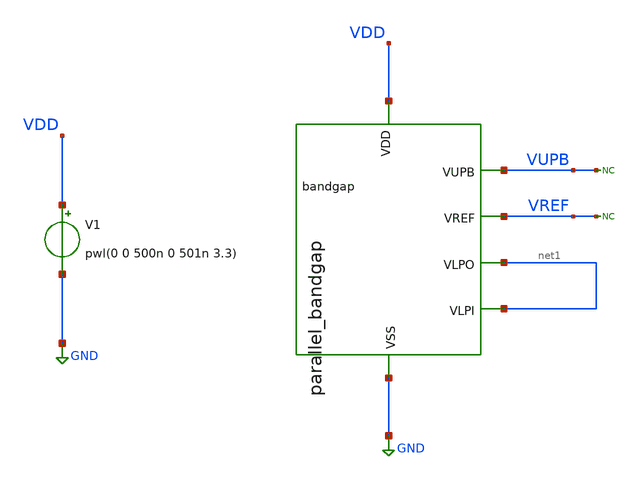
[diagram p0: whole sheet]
** sch_path: testbenches/parallel_bandgap_tran.sch
**.subckt parallel_bandgap_tran
bandgap VDD VUPB VREF net1 net1 GND parallel_bandgap
V1 VDD GND pwl(0 0 500n 0 501n 3.3)
.save i(v1)
* noconn VUPB
* noconn VREF
**.ends

* expanding   symbol:  parallel_bandgap.sym # of pins=6
** sym_path: designs/parallel_bandgap.sym
** sch_path: designs/parallel_bandgap.sch
.subckt parallel_bandgap VDD VUPB VREF VLPI VLPO VSS
*.ipin VDD
*.ipin VSS
*.opin VUPB
*.opin VREF
*.opin VLPO
*.ipin VLPI
XM1 net3 VUPB VDD VDD sky130_fd_pr__pfet_01v8_lvt L=8 W=50 nf=1 ad='int((nf+1)/2) * W/nf * 0.29' as='int((nf+2)/2) * W/nf * 0.29'
+ pd='2*int((nf+1)/2) * (W/nf + 0.29)' ps='2*int((nf+2)/2) * (W/nf + 0.29)' nrd='0.29 / W' nrs='0.29 / W'
+ sa=0 sb=0 sd=0 mult=1 m=1
XM2 net2 VUPB VDD VDD sky130_fd_pr__pfet_01v8_lvt L=8 W=50 nf=1 ad='int((nf+1)/2) * W/nf * 0.29' as='int((nf+2)/2) * W/nf * 0.29'
+ pd='2*int((nf+1)/2) * (W/nf + 0.29)' ps='2*int((nf+2)/2) * (W/nf + 0.29)' nrd='0.29 / W' nrs='0.29 / W'
+ sa=0 sb=0 sd=0 mult=1 m=1
XQ1 net12 VLPI net1 VSS sky130_fd_pr__npn_05v5_w1p00l2p00
XQ2 net11 VLPO VSS VSS sky130_fd_pr__npn_05v5_w1p00l2p00
XR1 VSS net1 VSS sky130_fd_pr__res_high_po_1p41 L=260 mult=1 m=1
XQ3 net4 VBE VSS VSS sky130_fd_pr__npn_05v5_w1p00l2p00
XR2 VSS VBE VSS sky130_fd_pr__res_high_po_1p41 L=2400 mult=1 m=1
XM4 VBE VCCAS net6 VDD sky130_fd_pr__pfet_01v8_lvt L=8 W=50 nf=1 ad='int((nf+1)/2) * W/nf * 0.29' as='int((nf+2)/2) * W/nf * 0.29'
+ pd='2*int((nf+1)/2) * (W/nf + 0.29)' ps='2*int((nf+2)/2) * (W/nf + 0.29)' nrd='0.29 / W' nrs='0.29 / W'
+ sa=0 sb=0 sd=0 mult=1 m=1
XM5 VCBIAS VCCAS net5 VDD sky130_fd_pr__pfet_01v8_lvt L=8 W=50 nf=1 ad='int((nf+1)/2) * W/nf * 0.29'
+ as='int((nf+2)/2) * W/nf * 0.29' pd='2*int((nf+1)/2) * (W/nf + 0.29)' ps='2*int((nf+2)/2) * (W/nf + 0.29)'
+ nrd='0.29 / W' nrs='0.29 / W' sa=0 sb=0 sd=0 mult=1 m=1
XM6 VCCAS net4 VSS VSS sky130_fd_pr__nfet_01v8 L=4 W=4 nf=1 ad='int((nf+1)/2) * W/nf * 0.29' as='int((nf+2)/2) * W/nf * 0.29'
+ pd='2*int((nf+1)/2) * (W/nf + 0.29)' ps='2*int((nf+2)/2) * (W/nf + 0.29)' nrd='0.29 / W' nrs='0.29 / W'
+ sa=0 sb=0 sd=0 mult=1 m=1
XR3 VSS VREF VSS sky130_fd_pr__res_high_po_1p41 L=2640 mult=1 m=1
XM8 VREF VCCAS net7 VDD sky130_fd_pr__pfet_01v8_lvt L=8 W=50 nf=1 ad='int((nf+1)/2) * W/nf * 0.29' as='int((nf+2)/2) * W/nf * 0.29'
+ pd='2*int((nf+1)/2) * (W/nf + 0.29)' ps='2*int((nf+2)/2) * (W/nf + 0.29)' nrd='0.29 / W' nrs='0.29 / W'
+ sa=0 sb=0 sd=0 mult=1 m=1
XM3 VUPB VPCAS net3 VDD sky130_fd_pr__pfet_01v8_lvt L=8 W=50 nf=1 ad='int((nf+1)/2) * W/nf * 0.29' as='int((nf+2)/2) * W/nf * 0.29'
+ pd='2*int((nf+1)/2) * (W/nf + 0.29)' ps='2*int((nf+2)/2) * (W/nf + 0.29)' nrd='0.29 / W' nrs='0.29 / W'
+ sa=0 sb=0 sd=0 mult=4 m=4
XM7 net10 VPCAS net2 VDD sky130_fd_pr__pfet_01v8_lvt L=8 W=50 nf=1 ad='int((nf+1)/2) * W/nf * 0.29' as='int((nf+2)/2) * W/nf * 0.29'
+ pd='2*int((nf+1)/2) * (W/nf + 0.29)' ps='2*int((nf+2)/2) * (W/nf + 0.29)' nrd='0.29 / W' nrs='0.29 / W'
+ sa=0 sb=0 sd=0 mult=4 m=4
XM9 net9 VUPB VDD VDD sky130_fd_pr__pfet_01v8_lvt L=8 W=50 nf=1 ad='int((nf+1)/2) * W/nf * 0.29' as='int((nf+2)/2) * W/nf * 0.29'
+ pd='2*int((nf+1)/2) * (W/nf + 0.29)' ps='2*int((nf+2)/2) * (W/nf + 0.29)' nrd='0.29 / W' nrs='0.29 / W'
+ sa=0 sb=0 sd=0 mult=1 m=1
XM10 net4 VPCAS net9 VDD sky130_fd_pr__pfet_01v8_lvt L=8 W=50 nf=1 ad='int((nf+1)/2) * W/nf * 0.29' as='int((nf+2)/2) * W/nf * 0.29'
+ pd='2*int((nf+1)/2) * (W/nf + 0.29)' ps='2*int((nf+2)/2) * (W/nf + 0.29)' nrd='0.29 / W' nrs='0.29 / W'
+ sa=0 sb=0 sd=0 mult=4 m=4
XM11 net8 VUPB VDD VDD sky130_fd_pr__pfet_01v8_lvt L=8 W=50 nf=1 ad='int((nf+1)/2) * W/nf * 0.29' as='int((nf+2)/2) * W/nf * 0.29'
+ pd='2*int((nf+1)/2) * (W/nf + 0.29)' ps='2*int((nf+2)/2) * (W/nf + 0.29)' nrd='0.29 / W' nrs='0.29 / W'
+ sa=0 sb=0 sd=0 mult=1 m=1
XM12 VREF VPCAS net8 VDD sky130_fd_pr__pfet_01v8_lvt L=8 W=50 nf=1 ad='int((nf+1)/2) * W/nf * 0.29' as='int((nf+2)/2) * W/nf * 0.29'
+ pd='2*int((nf+1)/2) * (W/nf + 0.29)' ps='2*int((nf+2)/2) * (W/nf + 0.29)' nrd='0.29 / W' nrs='0.29 / W'
+ sa=0 sb=0 sd=0 mult=4 m=4
XM13 net5 VCBIAS VDD VDD sky130_fd_pr__pfet_01v8_lvt L=8 W=50 nf=1 ad='int((nf+1)/2) * W/nf * 0.29' as='int((nf+2)/2) * W/nf * 0.29'
+ pd='2*int((nf+1)/2) * (W/nf + 0.29)' ps='2*int((nf+2)/2) * (W/nf + 0.29)' nrd='0.29 / W' nrs='0.29 / W'
+ sa=0 sb=0 sd=0 mult=1 m=1
XM14 net6 VCBIAS VDD VDD sky130_fd_pr__pfet_01v8_lvt L=8 W=50 nf=1 ad='int((nf+1)/2) * W/nf * 0.29' as='int((nf+2)/2) * W/nf * 0.29'
+ pd='2*int((nf+1)/2) * (W/nf + 0.29)' ps='2*int((nf+2)/2) * (W/nf + 0.29)' nrd='0.29 / W' nrs='0.29 / W'
+ sa=0 sb=0 sd=0 mult=1 m=1
XR5 VCCAS VCBIAS VSS sky130_fd_pr__res_high_po_1p41 L=700 mult=1 m=1
XM15 net7 VCBIAS VDD VDD sky130_fd_pr__pfet_01v8_lvt L=8 W=50 nf=1 ad='int((nf+1)/2) * W/nf * 0.29' as='int((nf+2)/2) * W/nf * 0.29'
+ pd='2*int((nf+1)/2) * (W/nf + 0.29)' ps='2*int((nf+2)/2) * (W/nf + 0.29)' nrd='0.29 / W' nrs='0.29 / W'
+ sa=0 sb=0 sd=0 mult=1 m=1
XR7 VPCAS VUPB VSS sky130_fd_pr__res_high_po_1p41 L=800 mult=1 m=1
XR8 net13 net10 VSS sky130_fd_pr__res_high_po_1p41 L=800 mult=1 m=1
XM16 net13 VLPO net11 VSS sky130_fd_pr__nfet_05v0_nvt L=2 W=10 nf=1 ad='int((nf+1)/2) * W/nf * 0.29'
+ as='int((nf+2)/2) * W/nf * 0.29' pd='2*int((nf+1)/2) * (W/nf + 0.29)' ps='2*int((nf+2)/2) * (W/nf + 0.29)'
+ nrd='0.29 / W' nrs='0.29 / W' sa=0 sb=0 sd=0 mult=6 m=6
XM18 VPCAS VLPI net12 VSS sky130_fd_pr__nfet_05v0_nvt L=2 W=10 nf=1 ad='int((nf+1)/2) * W/nf * 0.29'
+ as='int((nf+2)/2) * W/nf * 0.29' pd='2*int((nf+1)/2) * (W/nf + 0.29)' ps='2*int((nf+2)/2) * (W/nf + 0.29)'
+ nrd='0.29 / W' nrs='0.29 / W' sa=0 sb=0 sd=0 mult=6 m=6
XM19 VDD net13 VLPO VSS sky130_fd_pr__nfet_05v0_nvt L=2 W=10 nf=1 ad='int((nf+1)/2) * W/nf * 0.29' as='int((nf+2)/2) * W/nf * 0.29'
+ pd='2*int((nf+1)/2) * (W/nf + 0.29)' ps='2*int((nf+2)/2) * (W/nf + 0.29)' nrd='0.29 / W' nrs='0.29 / W'
+ sa=0 sb=0 sd=0 mult=1 m=1
XR9 VBE net14 VSS sky130_fd_pr__res_high_po_1p41 L=2400 mult=1 m=1
XC1 net4 net14 sky130_fd_pr__cap_mim_m3_1 W=10 L=10 MF=10 m=10
XM17 net17 VUPB VDD VDD sky130_fd_pr__pfet_01v8_lvt L=8 W=50 nf=1 ad='int((nf+1)/2) * W/nf * 0.29' as='int((nf+2)/2) * W/nf * 0.29'
+ pd='2*int((nf+1)/2) * (W/nf + 0.29)' ps='2*int((nf+2)/2) * (W/nf + 0.29)' nrd='0.29 / W' nrs='0.29 / W'
+ sa=0 sb=0 sd=0 mult=1 m=1
XM20 net15 net17 VUPB VDD sky130_fd_pr__pfet_01v8_lvt L=8 W=10 nf=1 ad='int((nf+1)/2) * W/nf * 0.29'
+ as='int((nf+2)/2) * W/nf * 0.29' pd='2*int((nf+1)/2) * (W/nf + 0.29)' ps='2*int((nf+2)/2) * (W/nf + 0.29)'
+ nrd='0.29 / W' nrs='0.29 / W' sa=0 sb=0 sd=0 mult=1 m=1
XM21 VSS net16 net15 VDD sky130_fd_pr__pfet_01v8_lvt L=8 W=10 nf=1 ad='int((nf+1)/2) * W/nf * 0.29' as='int((nf+2)/2) * W/nf * 0.29'
+ pd='2*int((nf+1)/2) * (W/nf + 0.29)' ps='2*int((nf+2)/2) * (W/nf + 0.29)' nrd='0.29 / W' nrs='0.29 / W'
+ sa=0 sb=0 sd=0 mult=1 m=1
XR10 net16 net17 VSS sky130_fd_pr__res_xhigh_po_0p35 L=350 mult=1 m=1
XR11 VSS net16 VSS sky130_fd_pr__res_xhigh_po_0p35 L=350 mult=1 m=1
.ends

.GLOBAL GND
.end
